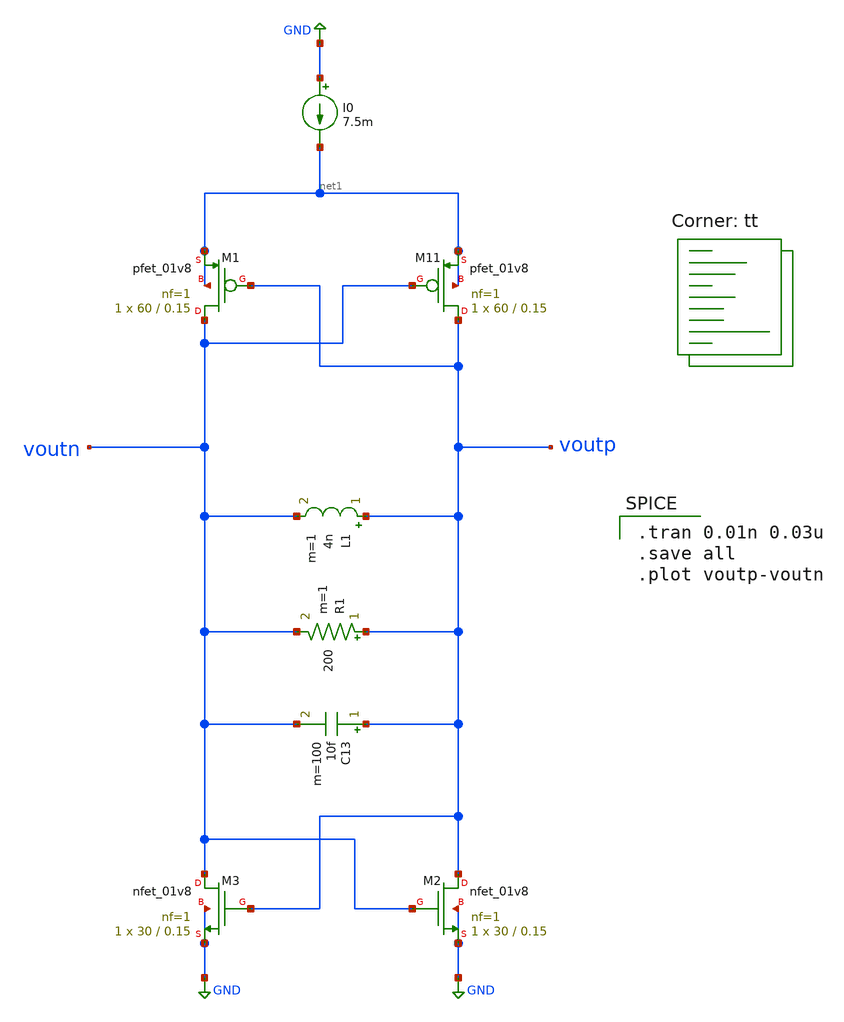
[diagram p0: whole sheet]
** sch_path: pll/lc_vco_lib_Ahmed_Reda/VCO_CMOS_init_tb/xschem/VCO_CMOS_init_tb.sch
**.subckt VCO_CMOS_init_tb
XM11 voutp voutn net1 net1 sky130_fd_pr__pfet_01v8 L=0.15 W=60 nf=1 ad='int((nf+1)/2) * W/nf * 0.29'
+ as='int((nf+2)/2) * W/nf * 0.29' pd='2*int((nf+1)/2) * (W/nf + 0.29)' ps='2*int((nf+2)/2) * (W/nf + 0.29)'
+ nrd='0.29 / W' nrs='0.29 / W' sa=0 sb=0 sd=0 mult=1 m=1
XM1 voutn voutp net1 net1 sky130_fd_pr__pfet_01v8 L=0.15 W=60 nf=1 ad='int((nf+1)/2) * W/nf * 0.29' as='int((nf+2)/2) * W/nf * 0.29'
+ pd='2*int((nf+1)/2) * (W/nf + 0.29)' ps='2*int((nf+2)/2) * (W/nf + 0.29)' nrd='0.29 / W' nrs='0.29 / W'
+ sa=0 sb=0 sd=0 mult=1 m=1
XM2 voutp voutn GND GND sky130_fd_pr__nfet_01v8 L=0.15 W=30 nf=1 ad='int((1 + 1)/2) * 30 / 1 * 0.29'
+ as='int((1 + 2)/2) * 30 / 1 * 0.29' pd='2*int((1 + 1)/2) * (30 / 1 + 0.29)' ps='2*int((1 + 2)/2) * (30 / 1 + 0.29)'
+ nrd='0.29 / 30 ' nrs='0.29 / 30 ' sa=0 sb=0 sd=0 mult=1 m=1
XM3 voutn voutp GND GND sky130_fd_pr__nfet_01v8 L=0.15 W=30 nf=1 ad='int((1 + 1)/2) * 30 / 1 * 0.29'
+ as='int((1 + 2)/2) * 30 / 1 * 0.29' pd='2*int((1 + 1)/2) * (30 / 1 + 0.29)' ps='2*int((1 + 2)/2) * (30 / 1 + 0.29)'
+ nrd='0.29 / 30 ' nrs='0.29 / 30 ' sa=0 sb=0 sd=0 mult=1 m=1
L1 voutp voutn 4n m=1
I0 GND net1 7.5m
C13 voutp voutn 10f m=100
R1 voutp voutn 200 m=1
**** begin user architecture code
.lib $::SKYWATER_MODELS/sky130.lib.spice tt

.tran 0.01n 0.03u
.save all
.plot voutp-voutn


** opencircuitdesign pdks install
.lib $::SKYWATER_MODELS/sky130.lib.spice tt


**** end user architecture code
**.ends
.GLOBAL GND
.end
